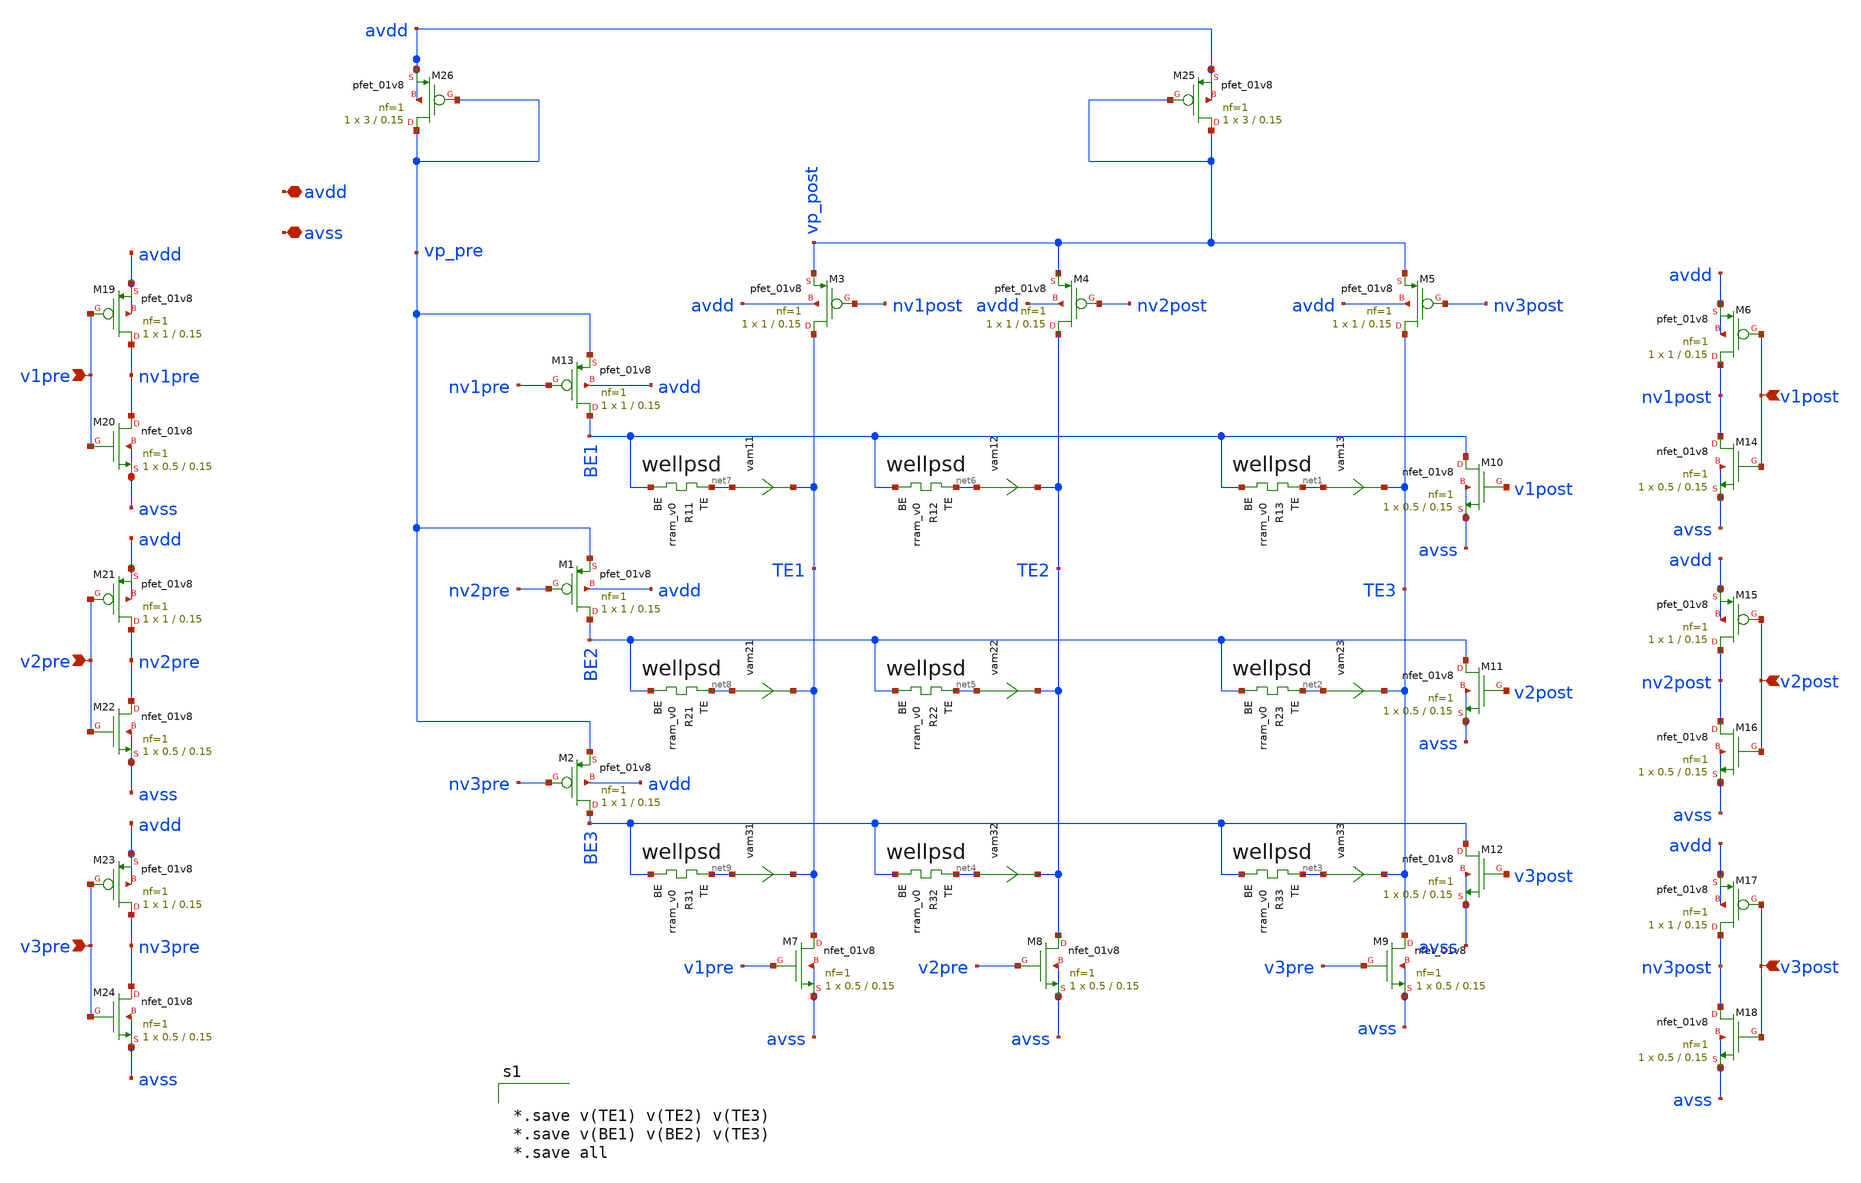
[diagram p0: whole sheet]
** sch_path: Synapse/cb_3x3_spk.sch
**.subckt cb_3x3_spk avdd avss v1post v2post v3post v1pre v2pre v3pre
*.iopin avdd
*.iopin avss
*.ipin v1post
*.ipin v2post
*.ipin v3post
*.ipin v1pre
*.ipin v2pre
*.ipin v3pre
XR13 net1 BE1 rram_v0
XM7 TE1 v1pre avss avss sky130_fd_pr__nfet_01v8 L=0.15 W=0.5 nf=1 ad='int((1 + 1)/2) * 0.5 / 1 * 0.29'
+ as='int((1 + 2)/2) * 0.5 / 1 * 0.29' pd='2*int((1 + 1)/2) * (0.5 / 1 + 0.29)' ps='2*int((1 + 2)/2) * (0.5 / 1 + 0.29)'
+ nrd='0.29 / 0.5 ' nrs='0.29 / 0.5 ' sa=0 sb=0 sd=0 mult=1 m=1
XM8 TE2 v2pre avss avss sky130_fd_pr__nfet_01v8 L=0.15 W=0.5 nf=1 ad='int((1 + 1)/2) * 0.5 / 1 * 0.29'
+ as='int((1 + 2)/2) * 0.5 / 1 * 0.29' pd='2*int((1 + 1)/2) * (0.5 / 1 + 0.29)' ps='2*int((1 + 2)/2) * (0.5 / 1 + 0.29)'
+ nrd='0.29 / 0.5 ' nrs='0.29 / 0.5 ' sa=0 sb=0 sd=0 mult=1 m=1
XM9 TE3 v3pre avss avss sky130_fd_pr__nfet_01v8 L=0.15 W=0.5 nf=1 ad='int((1 + 1)/2) * 0.5 / 1 * 0.29'
+ as='int((1 + 2)/2) * 0.5 / 1 * 0.29' pd='2*int((1 + 1)/2) * (0.5 / 1 + 0.29)' ps='2*int((1 + 2)/2) * (0.5 / 1 + 0.29)'
+ nrd='0.29 / 0.5 ' nrs='0.29 / 0.5 ' sa=0 sb=0 sd=0 mult=1 m=1
XM10 BE1 v1post avss avss sky130_fd_pr__nfet_01v8 L=0.15 W=0.5 nf=1 ad='int((1 + 1)/2) * 0.5 / 1 * 0.29'
+ as='int((1 + 2)/2) * 0.5 / 1 * 0.29' pd='2*int((1 + 1)/2) * (0.5 / 1 + 0.29)' ps='2*int((1 + 2)/2) * (0.5 / 1 + 0.29)'
+ nrd='0.29 / 0.5 ' nrs='0.29 / 0.5 ' sa=0 sb=0 sd=0 mult=1 m=1
XM11 BE2 v2post avss avss sky130_fd_pr__nfet_01v8 L=0.15 W=0.5 nf=1 ad='int((1 + 1)/2) * 0.5 / 1 * 0.29'
+ as='int((1 + 2)/2) * 0.5 / 1 * 0.29' pd='2*int((1 + 1)/2) * (0.5 / 1 + 0.29)' ps='2*int((1 + 2)/2) * (0.5 / 1 + 0.29)'
+ nrd='0.29 / 0.5 ' nrs='0.29 / 0.5 ' sa=0 sb=0 sd=0 mult=1 m=1
XM12 BE3 v3post avss avss sky130_fd_pr__nfet_01v8 L=0.15 W=0.5 nf=1 ad='int((1 + 1)/2) * 0.5 / 1 * 0.29'
+ as='int((1 + 2)/2) * 0.5 / 1 * 0.29' pd='2*int((1 + 1)/2) * (0.5 / 1 + 0.29)' ps='2*int((1 + 2)/2) * (0.5 / 1 + 0.29)'
+ nrd='0.29 / 0.5 ' nrs='0.29 / 0.5 ' sa=0 sb=0 sd=0 mult=1 m=1
XM13 BE1 nv1pre vp_pre avdd sky130_fd_pr__pfet_01v8 L=0.15 W=1 nf=1 ad='int((nf+1)/2) * W/nf * 0.29'
+ as='int((nf+2)/2) * W/nf * 0.29' pd='2*int((nf+1)/2) * (W/nf + 0.29)' ps='2*int((nf+2)/2) * (W/nf + 0.29)'
+ nrd='0.29 / W' nrs='0.29 / W' sa=0 sb=0 sd=0 mult=1 m=1
XM1 BE2 nv2pre vp_pre avdd sky130_fd_pr__pfet_01v8 L=0.15 W=1 nf=1 ad='int((nf+1)/2) * W/nf * 0.29' as='int((nf+2)/2) * W/nf * 0.29'
+ pd='2*int((nf+1)/2) * (W/nf + 0.29)' ps='2*int((nf+2)/2) * (W/nf + 0.29)' nrd='0.29 / W' nrs='0.29 / W'
+ sa=0 sb=0 sd=0 mult=1 m=1
XM2 BE3 nv3pre vp_pre avdd sky130_fd_pr__pfet_01v8 L=0.15 W=1 nf=1 ad='int((nf+1)/2) * W/nf * 0.29' as='int((nf+2)/2) * W/nf * 0.29'
+ pd='2*int((nf+1)/2) * (W/nf + 0.29)' ps='2*int((nf+2)/2) * (W/nf + 0.29)' nrd='0.29 / W' nrs='0.29 / W'
+ sa=0 sb=0 sd=0 mult=1 m=1
XM3 TE1 nv1post vp_post avdd sky130_fd_pr__pfet_01v8 L=0.15 W=1 nf=1 ad='int((nf+1)/2) * W/nf * 0.29'
+ as='int((nf+2)/2) * W/nf * 0.29' pd='2*int((nf+1)/2) * (W/nf + 0.29)' ps='2*int((nf+2)/2) * (W/nf + 0.29)'
+ nrd='0.29 / W' nrs='0.29 / W' sa=0 sb=0 sd=0 mult=1 m=1
XM4 TE2 nv2post vp_post avdd sky130_fd_pr__pfet_01v8 L=0.15 W=1 nf=1 ad='int((nf+1)/2) * W/nf * 0.29'
+ as='int((nf+2)/2) * W/nf * 0.29' pd='2*int((nf+1)/2) * (W/nf + 0.29)' ps='2*int((nf+2)/2) * (W/nf + 0.29)'
+ nrd='0.29 / W' nrs='0.29 / W' sa=0 sb=0 sd=0 mult=1 m=1
XM5 TE3 nv3post vp_post avdd sky130_fd_pr__pfet_01v8 L=0.15 W=1 nf=1 ad='int((nf+1)/2) * W/nf * 0.29'
+ as='int((nf+2)/2) * W/nf * 0.29' pd='2*int((nf+1)/2) * (W/nf + 0.29)' ps='2*int((nf+2)/2) * (W/nf + 0.29)'
+ nrd='0.29 / W' nrs='0.29 / W' sa=0 sb=0 sd=0 mult=1 m=1
XM6 nv1post v1post avdd avdd sky130_fd_pr__pfet_01v8 L=0.15 W=1 nf=1 ad='int((nf+1)/2) * W/nf * 0.29'
+ as='int((nf+2)/2) * W/nf * 0.29' pd='2*int((nf+1)/2) * (W/nf + 0.29)' ps='2*int((nf+2)/2) * (W/nf + 0.29)'
+ nrd='0.29 / W' nrs='0.29 / W' sa=0 sb=0 sd=0 mult=1 m=1
XM14 nv1post v1post avss avss sky130_fd_pr__nfet_01v8 L=0.15 W=0.5 nf=1 ad='int((1 + 1)/2) * 0.5 / 1 * 0.29'
+ as='int((1 + 2)/2) * 0.5 / 1 * 0.29' pd='2*int((1 + 1)/2) * (0.5 / 1 + 0.29)' ps='2*int((1 + 2)/2) * (0.5 / 1 + 0.29)'
+ nrd='0.29 / 0.5 ' nrs='0.29 / 0.5 ' sa=0 sb=0 sd=0 mult=1 m=1
XM15 nv2post v2post avdd avdd sky130_fd_pr__pfet_01v8 L=0.15 W=1 nf=1 ad='int((nf+1)/2) * W/nf * 0.29'
+ as='int((nf+2)/2) * W/nf * 0.29' pd='2*int((nf+1)/2) * (W/nf + 0.29)' ps='2*int((nf+2)/2) * (W/nf + 0.29)'
+ nrd='0.29 / W' nrs='0.29 / W' sa=0 sb=0 sd=0 mult=1 m=1
XM16 nv2post v2post avss avss sky130_fd_pr__nfet_01v8 L=0.15 W=0.5 nf=1 ad='int((1 + 1)/2) * 0.5 / 1 * 0.29'
+ as='int((1 + 2)/2) * 0.5 / 1 * 0.29' pd='2*int((1 + 1)/2) * (0.5 / 1 + 0.29)' ps='2*int((1 + 2)/2) * (0.5 / 1 + 0.29)'
+ nrd='0.29 / 0.5 ' nrs='0.29 / 0.5 ' sa=0 sb=0 sd=0 mult=1 m=1
XM17 nv3post v3post avdd avdd sky130_fd_pr__pfet_01v8 L=0.15 W=1 nf=1 ad='int((nf+1)/2) * W/nf * 0.29'
+ as='int((nf+2)/2) * W/nf * 0.29' pd='2*int((nf+1)/2) * (W/nf + 0.29)' ps='2*int((nf+2)/2) * (W/nf + 0.29)'
+ nrd='0.29 / W' nrs='0.29 / W' sa=0 sb=0 sd=0 mult=1 m=1
XM18 nv3post v3post avss avss sky130_fd_pr__nfet_01v8 L=0.15 W=0.5 nf=1 ad='int((1 + 1)/2) * 0.5 / 1 * 0.29'
+ as='int((1 + 2)/2) * 0.5 / 1 * 0.29' pd='2*int((1 + 1)/2) * (0.5 / 1 + 0.29)' ps='2*int((1 + 2)/2) * (0.5 / 1 + 0.29)'
+ nrd='0.29 / 0.5 ' nrs='0.29 / 0.5 ' sa=0 sb=0 sd=0 mult=1 m=1
XM19 nv1pre v1pre avdd avdd sky130_fd_pr__pfet_01v8 L=0.15 W=1 nf=1 ad='int((nf+1)/2) * W/nf * 0.29'
+ as='int((nf+2)/2) * W/nf * 0.29' pd='2*int((nf+1)/2) * (W/nf + 0.29)' ps='2*int((nf+2)/2) * (W/nf + 0.29)'
+ nrd='0.29 / W' nrs='0.29 / W' sa=0 sb=0 sd=0 mult=1 m=1
XM20 nv1pre v1pre avss avss sky130_fd_pr__nfet_01v8 L=0.15 W=0.5 nf=1 ad='int((1 + 1)/2) * 0.5 / 1 * 0.29'
+ as='int((1 + 2)/2) * 0.5 / 1 * 0.29' pd='2*int((1 + 1)/2) * (0.5 / 1 + 0.29)' ps='2*int((1 + 2)/2) * (0.5 / 1 + 0.29)'
+ nrd='0.29 / 0.5 ' nrs='0.29 / 0.5 ' sa=0 sb=0 sd=0 mult=1 m=1
XM21 nv2pre v2pre avdd avdd sky130_fd_pr__pfet_01v8 L=0.15 W=1 nf=1 ad='int((nf+1)/2) * W/nf * 0.29'
+ as='int((nf+2)/2) * W/nf * 0.29' pd='2*int((nf+1)/2) * (W/nf + 0.29)' ps='2*int((nf+2)/2) * (W/nf + 0.29)'
+ nrd='0.29 / W' nrs='0.29 / W' sa=0 sb=0 sd=0 mult=1 m=1
XM22 nv2pre v2pre avss avss sky130_fd_pr__nfet_01v8 L=0.15 W=0.5 nf=1 ad='int((1 + 1)/2) * 0.5 / 1 * 0.29'
+ as='int((1 + 2)/2) * 0.5 / 1 * 0.29' pd='2*int((1 + 1)/2) * (0.5 / 1 + 0.29)' ps='2*int((1 + 2)/2) * (0.5 / 1 + 0.29)'
+ nrd='0.29 / 0.5 ' nrs='0.29 / 0.5 ' sa=0 sb=0 sd=0 mult=1 m=1
XM23 nv3pre v3pre avdd avdd sky130_fd_pr__pfet_01v8 L=0.15 W=1 nf=1 ad='int((nf+1)/2) * W/nf * 0.29'
+ as='int((nf+2)/2) * W/nf * 0.29' pd='2*int((nf+1)/2) * (W/nf + 0.29)' ps='2*int((nf+2)/2) * (W/nf + 0.29)'
+ nrd='0.29 / W' nrs='0.29 / W' sa=0 sb=0 sd=0 mult=1 m=1
XM24 nv3pre v3pre avss avss sky130_fd_pr__nfet_01v8 L=0.15 W=0.5 nf=1 ad='int((1 + 1)/2) * 0.5 / 1 * 0.29'
+ as='int((1 + 2)/2) * 0.5 / 1 * 0.29' pd='2*int((1 + 1)/2) * (0.5 / 1 + 0.29)' ps='2*int((1 + 2)/2) * (0.5 / 1 + 0.29)'
+ nrd='0.29 / 0.5 ' nrs='0.29 / 0.5 ' sa=0 sb=0 sd=0 mult=1 m=1
vam13 net1 TE3 0
.save i(vam13)
XR23 net2 BE2 rram_v0
vam23 net2 TE3 0
.save i(vam23)
XR33 net3 BE3 rram_v0
vam33 net3 TE3 0
.save i(vam33)
XR32 net4 BE3 rram_v0
vam32 net4 TE2 0
.save i(vam32)
XR22 net5 BE2 rram_v0
vam22 net5 TE2 0
.save i(vam22)
XR12 net6 BE1 rram_v0
vam12 net6 TE2 0
.save i(vam12)
XR11 net7 BE1 rram_v0
vam11 net7 TE1 0
.save i(vam11)
XR21 net8 BE2 rram_v0
vam21 net8 TE1 0
.save i(vam21)
XR31 net9 BE3 rram_v0
vam31 net9 TE1 0
.save i(vam31)
XM25 vp_post vp_post avdd avdd sky130_fd_pr__pfet_01v8 L=0.15 W=3 nf=1 ad='int((nf+1)/2) * W/nf * 0.29'
+ as='int((nf+2)/2) * W/nf * 0.29' pd='2*int((nf+1)/2) * (W/nf + 0.29)' ps='2*int((nf+2)/2) * (W/nf + 0.29)'
+ nrd='0.29 / W' nrs='0.29 / W' sa=0 sb=0 sd=0 mult=1 m=1
XM26 vp_pre vp_pre avdd avdd sky130_fd_pr__pfet_01v8 L=0.15 W=3 nf=1 ad='int((nf+1)/2) * W/nf * 0.29'
+ as='int((nf+2)/2) * W/nf * 0.29' pd='2*int((nf+1)/2) * (W/nf + 0.29)' ps='2*int((nf+2)/2) * (W/nf + 0.29)'
+ nrd='0.29 / W' nrs='0.29 / W' sa=0 sb=0 sd=0 mult=1 m=1
**** begin user architecture code


*.save v(TE1) v(TE2) v(TE3)
*.save v(BE1) v(BE2) v(TE3)
*.save all


**** end user architecture code
**.ends
.end
